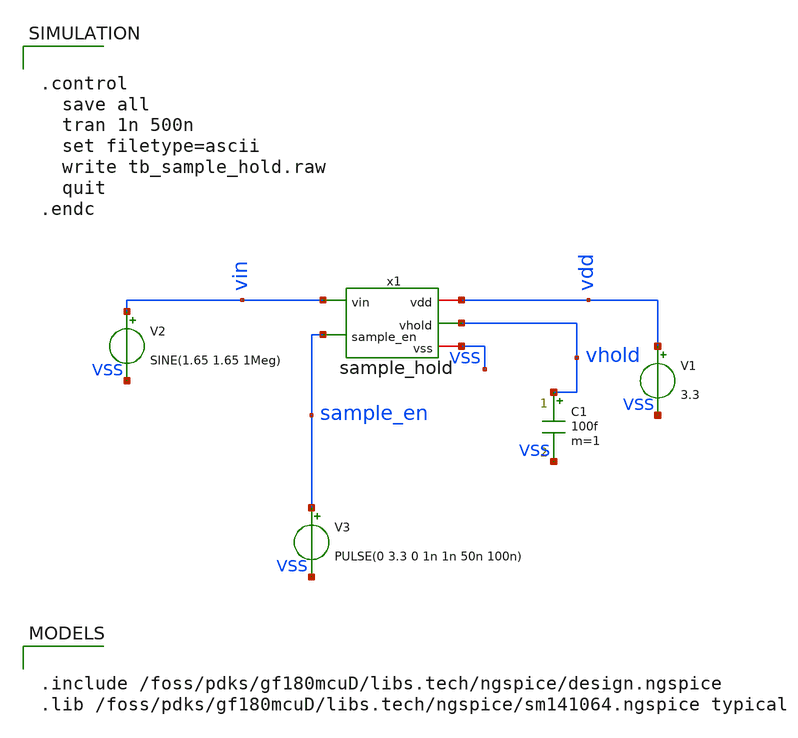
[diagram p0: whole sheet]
** sch_path: xschem/sar_adc/blocks/sample_hold/testbench/tb_sample_hold.sch
**.subckt tb_sample_hold
V1 vdd VSS 3.3
V2 vin VSS SINE(1.65 1.65 1Meg)
V3 sample_en VSS PULSE(0 3.3 0 1n 1n 50n 100n)
C1 vhold VSS 100f m=1
x1 vin sample_en vhold vdd VSS sample_hold
**** begin user architecture code


.include /foss/pdks/gf180mcuD/libs.tech/ngspice/design.ngspice
.lib /foss/pdks/gf180mcuD/libs.tech/ngspice/sm141064.ngspice typical




.control
  save all
  tran 1n 500n
  set filetype=ascii
  write tb_sample_hold.raw
  quit
.endc


**** end user architecture code
**.ends
.end
